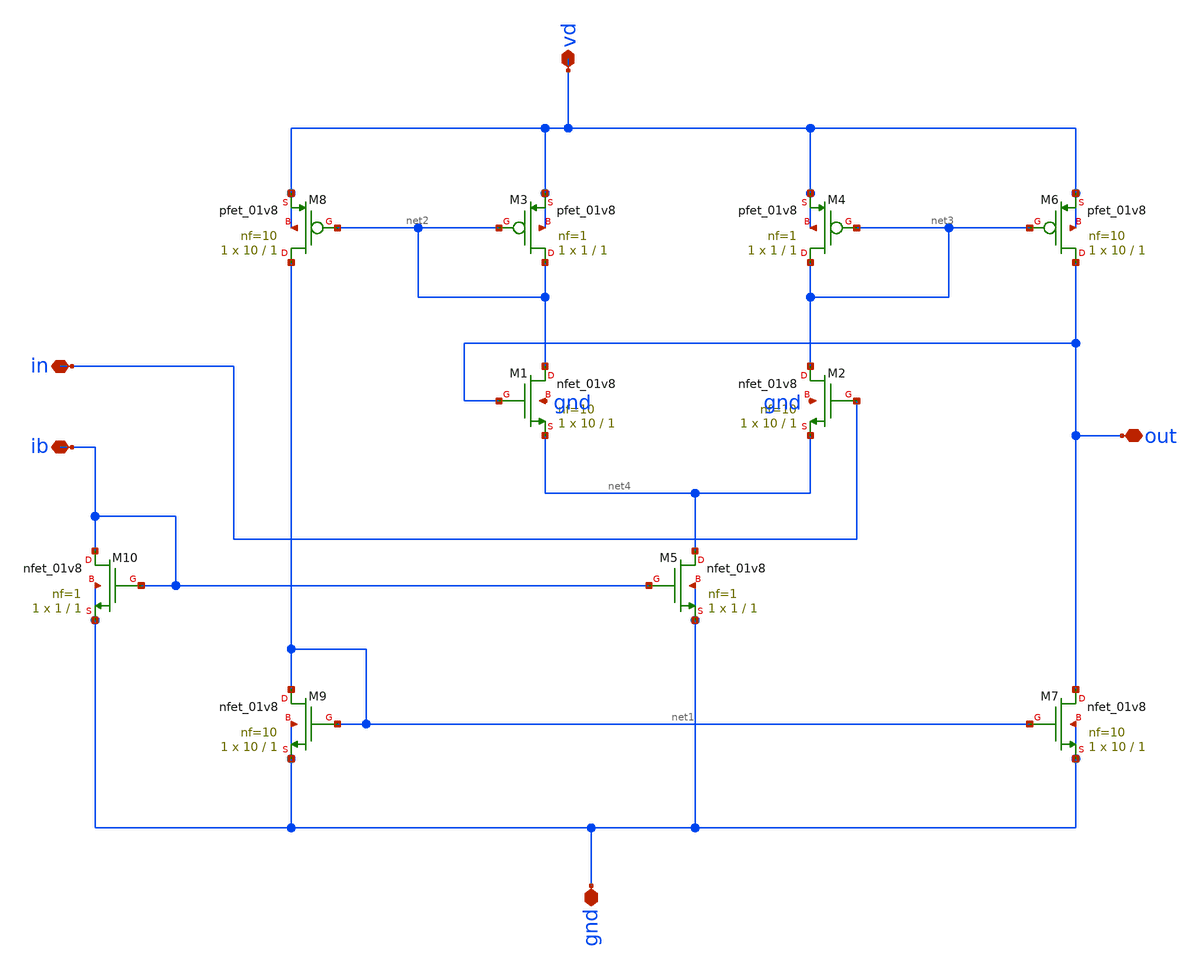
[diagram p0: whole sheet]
** sch_path: amp-op/xschem/buffer.sch
* Copyright 2020 Stefan Frederik Schippers
* Licensed under the Apache License, Version 2.0 (the "License");
* you may not use this file except in compliance with the License.
* You may obtain a copy of the License at
* https://www.apache.org/licenses/LICENSE-2.0
* Unless required by applicable law or agreed to in writing, software
* distributed under the License is distributed on an "AS IS" BASIS,
* WITHOUT WARRANTIES OR CONDITIONS OF ANY KIND, either express or implied.
* See the License for the specific language governing permissions and
* limitations under the License.
**.subckt buffer vd ib out in gnd
*.iopin vd
*.iopin ib
*.iopin out
*.iopin in
*.iopin gnd
XM3 net2 net2 vd vd sky130_fd_pr__pfet_01v8 L=1 W=1 nf=1 ad='int((nf+1)/2) * W/nf * 0.29' as='int((nf+2)/2) * W/nf * 0.29'
+ pd='2*int((nf+1)/2) * (W/nf + 0.29)' ps='2*int((nf+2)/2) * (W/nf + 0.29)' nrd='0.29 / W' nrs='0.29 / W'
+ sa=0 sb=0 sd=0 mult=1 m=1
XM1 net2 out net4 gnd sky130_fd_pr__nfet_01v8 L=1 W=10 nf=10 ad='int((nf+1)/2) * W/nf * 0.29' as='int((nf+2)/2) * W/nf * 0.29'
+ pd='2*int((nf+1)/2) * (W/nf + 0.29)' ps='2*int((nf+2)/2) * (W/nf + 0.29)' nrd='0.29 / W' nrs='0.29 / W'
+ sa=0 sb=0 sd=0 mult=1 m=1
XM2 net3 in net4 gnd sky130_fd_pr__nfet_01v8 L=1 W=10 nf=10 ad='int((nf+1)/2) * W/nf * 0.29' as='int((nf+2)/2) * W/nf * 0.29'
+ pd='2*int((nf+1)/2) * (W/nf + 0.29)' ps='2*int((nf+2)/2) * (W/nf + 0.29)' nrd='0.29 / W' nrs='0.29 / W'
+ sa=0 sb=0 sd=0 mult=1 m=1
XM4 net3 net3 vd vd sky130_fd_pr__pfet_01v8 L=1 W=1 nf=1 ad='int((nf+1)/2) * W/nf * 0.29' as='int((nf+2)/2) * W/nf * 0.29'
+ pd='2*int((nf+1)/2) * (W/nf + 0.29)' ps='2*int((nf+2)/2) * (W/nf + 0.29)' nrd='0.29 / W' nrs='0.29 / W'
+ sa=0 sb=0 sd=0 mult=1 m=1
XM5 net4 ib gnd gnd sky130_fd_pr__nfet_01v8 L=1 W=1 nf=1 ad='int((nf+1)/2) * W/nf * 0.29' as='int((nf+2)/2) * W/nf * 0.29'
+ pd='2*int((nf+1)/2) * (W/nf + 0.29)' ps='2*int((nf+2)/2) * (W/nf + 0.29)' nrd='0.29 / W' nrs='0.29 / W'
+ sa=0 sb=0 sd=0 mult=1 m=1
XM6 out net3 vd vd sky130_fd_pr__pfet_01v8 L=1 W=10 nf=10 ad='int((nf+1)/2) * W/nf * 0.29' as='int((nf+2)/2) * W/nf * 0.29'
+ pd='2*int((nf+1)/2) * (W/nf + 0.29)' ps='2*int((nf+2)/2) * (W/nf + 0.29)' nrd='0.29 / W' nrs='0.29 / W'
+ sa=0 sb=0 sd=0 mult=1 m=1
XM7 out net1 gnd gnd sky130_fd_pr__nfet_01v8 L=1 W=10 nf=10 ad='int((nf+1)/2) * W/nf * 0.29' as='int((nf+2)/2) * W/nf * 0.29'
+ pd='2*int((nf+1)/2) * (W/nf + 0.29)' ps='2*int((nf+2)/2) * (W/nf + 0.29)' nrd='0.29 / W' nrs='0.29 / W'
+ sa=0 sb=0 sd=0 mult=1 m=1
XM8 net1 net2 vd vd sky130_fd_pr__pfet_01v8 L=1 W=10 nf=10 ad='int((nf+1)/2) * W/nf * 0.29' as='int((nf+2)/2) * W/nf * 0.29'
+ pd='2*int((nf+1)/2) * (W/nf + 0.29)' ps='2*int((nf+2)/2) * (W/nf + 0.29)' nrd='0.29 / W' nrs='0.29 / W'
+ sa=0 sb=0 sd=0 mult=1 m=1
XM9 net1 net1 gnd gnd sky130_fd_pr__nfet_01v8 L=1 W=10 nf=10 ad='int((nf+1)/2) * W/nf * 0.29' as='int((nf+2)/2) * W/nf * 0.29'
+ pd='2*int((nf+1)/2) * (W/nf + 0.29)' ps='2*int((nf+2)/2) * (W/nf + 0.29)' nrd='0.29 / W' nrs='0.29 / W'
+ sa=0 sb=0 sd=0 mult=1 m=1
XM10 ib ib gnd gnd sky130_fd_pr__nfet_01v8 L=1 W=1 nf=1 ad='int((nf+1)/2) * W/nf * 0.29' as='int((nf+2)/2) * W/nf * 0.29'
+ pd='2*int((nf+1)/2) * (W/nf + 0.29)' ps='2*int((nf+2)/2) * (W/nf + 0.29)' nrd='0.29 / W' nrs='0.29 / W'
+ sa=0 sb=0 sd=0 mult=1 m=1
**** begin user architecture code

R0 in.n1 in.n0 150.875
R1 in.n5 in.n4 150.49
R2 in.n3 in.n2 150.488
R3 in.n7 in.n6 141.16
R4 in.n0 in.t9 25.228
R5 in.n6 in.t7 24.105
R6 in.n0 in.t2 24.104
R7 in.n2 in.t4 24.103
R8 in.n4 in.t0 24.102
R9 in.n1 in.t5 24.102
R10 in.n5 in.t8 24.102
R11 in.n3 in.t6 24.102
R12 in.n7 in.t3 24.102
R13 in.n9 in.t1 24.1
R14 in.n14 in.n13 9.3
R15 in in.n14 5.261
R16 in.n8 in.n7 1.785
R17 in.n2 in.n1 1.103
R18 in.n4 in.n3 1.094
R19 in.n6 in.n5 0.41
R20 in.n14 in.n12 0.076
R21 in.n12 in.n8 0.014
R22 in.n12 in.n11 0.005
R23 in.n10 in.n9 0.005
R24 in.n11 in.n10 0.001
R25 out.t0 out.n7 175.091
R26 out.n0 out.t2 175.044
R27 out.n2 out.n1 150.491
R28 out.n4 out.n3 150.491
R29 out.n6 out.n5 141.106
R30 out out.t0 26.91
R31 out.n5 out.t1 24.103
R32 out.n6 out.t7 24.103
R33 out.n4 out.t5 24.103
R34 out.n2 out.t3 24.102
R35 out.n0 out.t6 24.102
R36 out.n1 out.t9 24.102
R37 out.n3 out.t4 24.102
R38 out.n7 out.t8 24.102
R39 out.n7 out.n6 1.085
R40 out.n3 out.n2 0.988
R41 out.n5 out.n4 0.913
R42 out.n1 out.n0 0.863
R43 net2.n4 net2.t6 40.035
R44 net2.n0 net2.t11 40.035
R45 net2.n8 net2.t0 39.528
R46 net2.n7 net2.t4 39.528
R47 net2.n6 net2.t5 39.528
R48 net2.n5 net2.t3 39.528
R49 net2.n4 net2.t2 39.528
R50 net2.n3 net2.t9 39.528
R51 net2.n2 net2.t10 39.528
R52 net2.n1 net2.t8 39.528
R53 net2.n0 net2.t7 39.528
R54 net2.n10 net2.t1 28.57
R55 net2.n8 net2.n7 1.982
R56 net2.n9 net2.n3 1.708
R57 net2 net2.n10 0.985
R58 net2.n5 net2.n4 0.507
R59 net2.n6 net2.n5 0.507
R60 net2.n7 net2.n6 0.507
R61 net2.n1 net2.n0 0.507
R62 net2.n2 net2.n1 0.507
R63 net2.n3 net2.n2 0.507
R64 net2.n10 net2.n9 0.335
R65 net2.n9 net2.n8 0.303
R66 vd.n53 vd.n52 379.482
R67 vd.n40 vd.n34 379.482
R68 vd.n54 vd.n53 297.411
R69 vd.n41 vd.n40 297.411
R70 vd.n19 vd.n16 131.387
R71 vd.n4 vd.n1 131.387
R72 vd.n24 vd.n21 131.011
R73 vd.n9 vd.n6 131.011
R74 vd.n29 vd.n24 54.211
R75 vd.n14 vd.n9 54.211
R76 vd.n29 vd.n19 53.835
R77 vd.n14 vd.n4 53.835
R78 vd.n57 vd.n14 8.271
R79 vd.n57 vd.n29 7.938
R80 vd.n57 vd.n56 4.028
R81 vd.n55 vd.n45 0.296
R82 vd vd.n57 0.28
R83 vd.n42 vd.n32 0.228
R84 vd.n56 vd.n55 0.18
R85 vd.n56 vd.n42 0.167
R86 vd.n19 vd.n18 0.161
R87 vd.n24 vd.n23 0.161
R88 vd.n4 vd.n3 0.161
R89 vd.n9 vd.n8 0.161
R90 vd.n23 vd.n22 0.139
R91 vd.n8 vd.n7 0.139
R92 vd.n18 vd.n17 0.139
R93 vd.n3 vd.n2 0.139
R94 vd.n42 vd.n41 0.017
R95 vd.n55 vd.n54 0.017
R96 vd.n16 vd.n15 0.015
R97 vd.n21 vd.n20 0.015
R98 vd.n1 vd.n0 0.015
R99 vd.n6 vd.n5 0.015
R100 vd.n52 vd.n51 0.013
R101 vd.n34 vd.n33 0.013
R102 vd.n26 vd.n25 0.013
R103 vd.n27 vd.n26 0.013
R104 vd.n11 vd.n10 0.013
R105 vd.n12 vd.n11 0.013
R106 vd.n53 vd.n50 0.003
R107 vd.n47 vd.n46 0.003
R108 vd.n36 vd.n35 0.003
R109 vd.n40 vd.n39 0.003
R110 vd.n50 vd.n49 0.003
R111 vd.n37 vd.n36 0.003
R112 vd.n48 vd.n47 0.003
R113 vd.n39 vd.n38 0.003
R114 vd.n49 vd.n48 0.002
R115 vd.n38 vd.n37 0.002
R116 vd.n29 vd.n28 0.002
R117 vd.n28 vd.n27 0.002
R118 vd.n14 vd.n13 0.002
R119 vd.n13 vd.n12 0.002
R120 vd.n32 vd.n31 0.001
R121 vd.n45 vd.n44 0.001
R122 vd.n44 vd.n43 0.001
R123 vd.n31 vd.n30 0.001
R124 ib.n0 ib.t2 24.837
R125 ib.n0 ib.t0 24.107
R126 ib.n1 ib.t1 17.747
R127 ib ib.n1 1.062
R128 ib.n1 ib.n0 0.387
C0 in net1 0.88fF
C1 net1 out 1.67fF
C2 in out 1.39fF
C3 net1 net4 0.18fF
C4 ib net1 0.04fF
C5 net3 net1 0.47fF
C6 in net4 2.12fF
C7 out net4 2.13fF
C8 ib in 0.06fF
C9 ib out 0.00fF
C10 vd net1 2.04fF
C11 net3 in 1.40fF
C12 net3 out 2.33fF
C13 in vd 0.81fF
C14 vd out 1.79fF
C15 ib net4 0.04fF
C16 net3 net4 2.19fF
C17 net3 ib 0.01fF
C18 net2 net1 2.18fF
C19 vd net4 0.09fF
C20 ib vd 0.02fF
C21 net3 vd 3.38fF
C22 net2 in 0.55fF
C23 net2 out 2.13fF
C24 net2 net4 1.85fF
C25 net3 net2 0.62fF
C26 net2 vd 4.36fF
C27 vd.n0 gnd 0.41fF $ **FLOATING
C28 vd.n1 gnd 0.07fF $ **FLOATING
C29 vd.n2 gnd 0.39fF $ **FLOATING
C30 vd.n3 gnd 0.04fF $ **FLOATING
C31 vd.n4 gnd 0.04fF $ **FLOATING
C32 vd.n5 gnd 0.41fF $ **FLOATING
C33 vd.n6 gnd 0.07fF $ **FLOATING
C34 vd.n7 gnd 0.39fF $ **FLOATING
C35 vd.n8 gnd 0.04fF $ **FLOATING
C36 vd.n9 gnd 0.04fF $ **FLOATING
C37 vd.n10 gnd 0.09fF $ **FLOATING
C38 vd.n11 gnd 0.09fF $ **FLOATING
C39 vd.n12 gnd 0.43fF $ **FLOATING
C40 vd.n13 gnd 0.02fF $ **FLOATING
C41 vd.n14 gnd 0.59fF $ **FLOATING
C42 vd.n15 gnd 0.41fF $ **FLOATING
C43 vd.n16 gnd 0.07fF $ **FLOATING
C44 vd.n17 gnd 0.39fF $ **FLOATING
C45 vd.n18 gnd 0.04fF $ **FLOATING
C46 vd.n19 gnd 0.04fF $ **FLOATING
C47 vd.n20 gnd 0.41fF $ **FLOATING
C48 vd.n21 gnd 0.07fF $ **FLOATING
C49 vd.n22 gnd 0.39fF $ **FLOATING
C50 vd.n23 gnd 0.04fF $ **FLOATING
C51 vd.n24 gnd 0.04fF $ **FLOATING
C52 vd.n25 gnd 0.09fF $ **FLOATING
C53 vd.n26 gnd 0.09fF $ **FLOATING
C54 vd.n27 gnd 0.43fF $ **FLOATING
C55 vd.n28 gnd 0.02fF $ **FLOATING
C56 vd.n29 gnd 0.62fF $ **FLOATING
C57 vd.n30 gnd 1.56fF $ **FLOATING
C58 vd.n31 gnd 0.04fF $ **FLOATING
C59 vd.n32 gnd 0.77fF $ **FLOATING
C60 vd.n33 gnd 1.56fF $ **FLOATING
C61 vd.n34 gnd 0.18fF $ **FLOATING
C62 vd.n35 gnd 0.15fF $ **FLOATING
C63 vd.n36 gnd 0.17fF $ **FLOATING
C64 vd.n37 gnd 1.21fF $ **FLOATING
C65 vd.n38 gnd 1.21fF $ **FLOATING
C66 vd.n39 gnd 0.17fF $ **FLOATING
C67 vd.n40 gnd 0.15fF $ **FLOATING
C68 vd.n41 gnd 0.09fF $ **FLOATING
C69 vd.n42 gnd 0.12fF $ **FLOATING
C70 vd.n43 gnd 1.56fF $ **FLOATING
C71 vd.n44 gnd 0.04fF $ **FLOATING
C72 vd.n45 gnd 0.41fF $ **FLOATING
C73 vd.n46 gnd 0.15fF $ **FLOATING
C74 vd.n47 gnd 0.17fF $ **FLOATING
C75 vd.n48 gnd 1.21fF $ **FLOATING
C76 vd.n49 gnd 1.21fF $ **FLOATING
C77 vd.n50 gnd 0.17fF $ **FLOATING
C78 vd.n51 gnd 1.56fF $ **FLOATING
C79 vd.n52 gnd 0.18fF $ **FLOATING
C80 vd.n53 gnd 0.15fF $ **FLOATING
C81 vd.n54 gnd 0.09fF $ **FLOATING
C82 vd.n55 gnd 0.42fF $ **FLOATING
C83 vd.n56 gnd 1.70fF $ **FLOATING
C84 vd.n57 gnd 15.86fF $ **FLOATING
C85 net2.t11 gnd 0.65fF
C86 net2.t7 gnd 0.65fF
C87 net2.n0 gnd 0.82fF $ **FLOATING
C88 net2.t8 gnd 0.65fF
C89 net2.n1 gnd 0.42fF $ **FLOATING
C90 net2.t10 gnd 0.65fF
C91 net2.n2 gnd 0.42fF $ **FLOATING
C92 net2.t9 gnd 0.65fF
C93 net2.n3 gnd 0.53fF $ **FLOATING
C94 net2.t0 gnd 0.65fF
C95 net2.t4 gnd 0.65fF
C96 net2.t5 gnd 0.65fF
C97 net2.t3 gnd 0.65fF
C98 net2.t2 gnd 0.65fF
C99 net2.t6 gnd 0.65fF
C100 net2.n4 gnd 0.82fF $ **FLOATING
C101 net2.n5 gnd 0.42fF $ **FLOATING
C102 net2.n6 gnd 0.42fF $ **FLOATING
C103 net2.n7 gnd 0.56fF $ **FLOATING
C104 net2.n8 gnd 0.53fF $ **FLOATING
C105 net2.n9 gnd 0.23fF $ **FLOATING
C106 net2.t1 gnd 0.03fF
C107 net2.n10 gnd 0.37fF $ **FLOATING
C108 out.t8 gnd 0.59fF
C109 out.t1 gnd 0.59fF
C110 out.t4 gnd 0.59fF
C111 out.t9 gnd 0.59fF
C112 out.t2 gnd 0.95fF
C113 out.t6 gnd 0.59fF
C114 out.n0 gnd 2.73fF $ **FLOATING
C115 out.n1 gnd 2.86fF $ **FLOATING
C116 out.t3 gnd 0.59fF
C117 out.n2 gnd 0.87fF $ **FLOATING
C118 out.n3 gnd 0.87fF $ **FLOATING
C119 out.t5 gnd 0.59fF
C120 out.n4 gnd 0.92fF $ **FLOATING
C121 out.n5 gnd 0.93fF $ **FLOATING
C122 out.t7 gnd 0.59fF
C123 out.n6 gnd 0.85fF $ **FLOATING
C124 out.n7 gnd 0.92fF $ **FLOATING
C125 out.t0 gnd 0.62fF
C126 in.t0 gnd 0.41fF
C127 in.t5 gnd 0.41fF
C128 in.t9 gnd 0.44fF
C129 in.t2 gnd 0.41fF
C130 in.n0 gnd 1.13fF $ **FLOATING
C131 in.n1 gnd 0.58fF $ **FLOATING
C132 in.t4 gnd 0.41fF
C133 in.n2 gnd 0.58fF $ **FLOATING
C134 in.t6 gnd 0.41fF
C135 in.n3 gnd 0.59fF $ **FLOATING
C136 in.n4 gnd 0.58fF $ **FLOATING
C137 in.t8 gnd 0.41fF
C138 in.n5 gnd 0.69fF $ **FLOATING
C139 in.t7 gnd 0.41fF
C140 in.n6 gnd 0.69fF $ **FLOATING
C141 in.t3 gnd 0.41fF
C142 in.n7 gnd 0.49fF $ **FLOATING
C143 in.n8 gnd 0.22fF $ **FLOATING
C144 in.t1 gnd 0.41fF
C145 in.n9 gnd 0.17fF $ **FLOATING
C146 in.n10 gnd 0.00fF $ **FLOATING
C147 in.n11 gnd 0.01fF $ **FLOATING
C148 in.n12 gnd 0.02fF $ **FLOATING
C149 in.n13 gnd 0.02fF $ **FLOATING
C150 in.n14 gnd 0.25fF $ **FLOATING
C151 net4 gnd 1.49fF
C152 ib gnd 1.87fF
C153 out gnd 13.46fF
C154 net3 gnd 3.38fF
C155 vd gnd 18.59fF
C156 net1 gnd 17.83fF
C157 net2 gnd 8.89fF
C158 in gnd 6.08fF


**** end user architecture code
**.ends
.end
